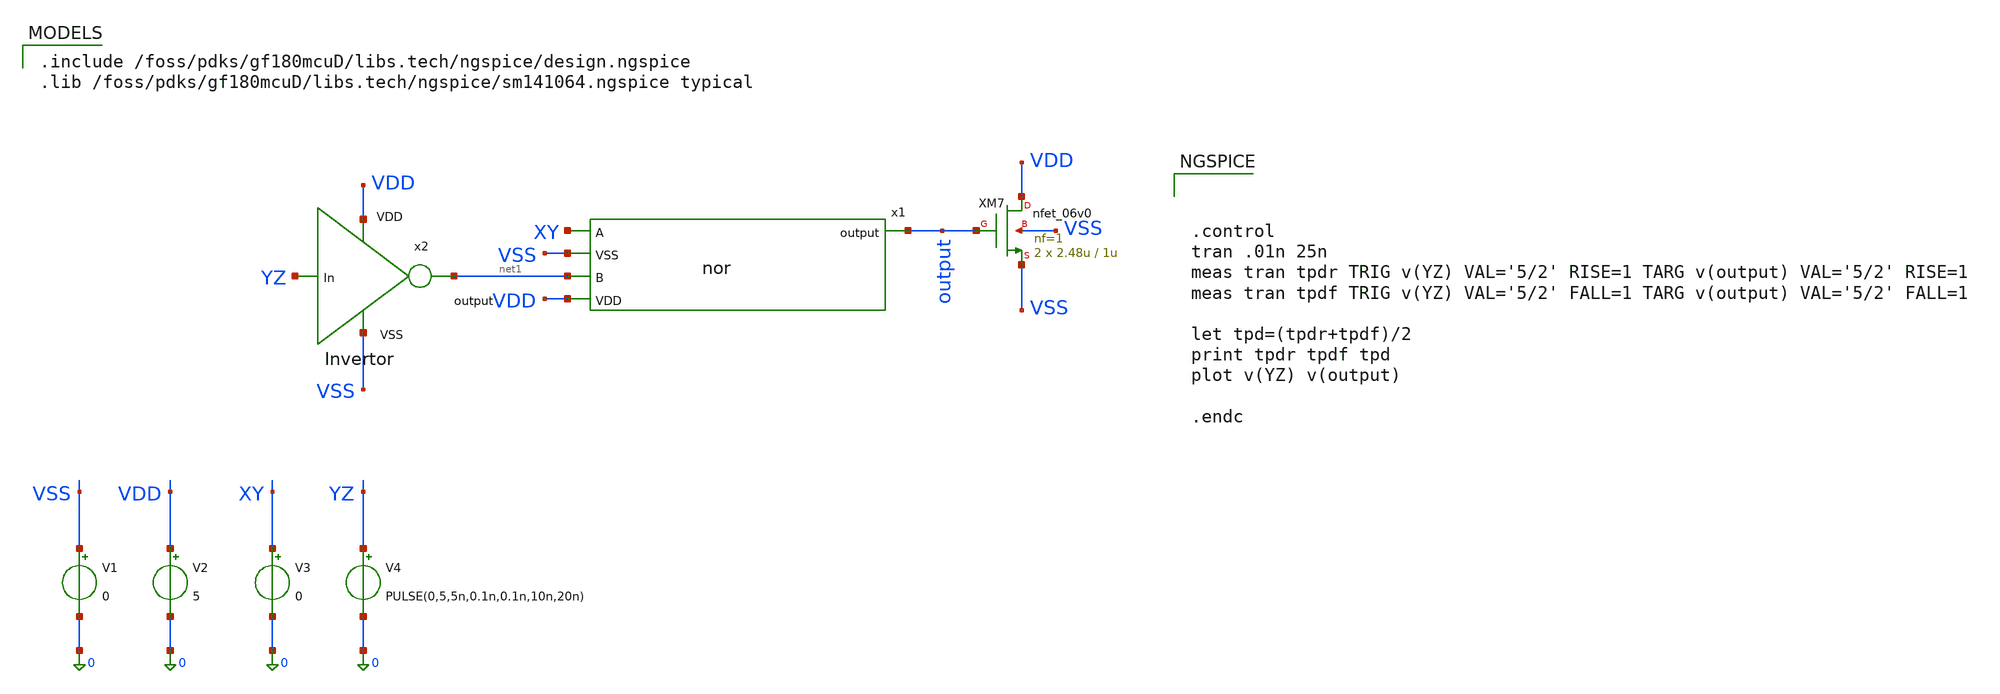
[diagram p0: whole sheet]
** sch_path: activities/opamp3AKAM/yDelayTBV2.sch
**.subckt yDelayTBV2
V1 VSS 0 0
V2 VDD 0 5
V3 XY 0 0
V4 YZ 0 PULSE(0,5,5n,0.1n,0.1n,10n,20n)
x1 XY VSS net1 output VDD nor
x2 VDD net1 YZ VSS invertor
XM7 VDD output VSS VSS nfet_06v0 L=1u W=2.48u nf=1 ad='int((nf+1)/2) * W/nf * 0.18u' as='int((nf+2)/2) * W/nf * 0.18u'
+ pd='2*int((nf+1)/2) * (W/nf + 0.18u)' ps='2*int((nf+2)/2) * (W/nf + 0.18u)' nrd='0.18u / W' nrs='0.18u / W'
+ sa=0 sb=0 sd=0 m=2
**** begin user architecture code

.include /foss/pdks/gf180mcuD/libs.tech/ngspice/design.ngspice
.lib /foss/pdks/gf180mcuD/libs.tech/ngspice/sm141064.ngspice typical




.control
tran .01n 25n
meas tran tpdr TRIG v(YZ) VAL='5/2' RISE=1 TARG v(output) VAL='5/2' RISE=1
meas tran tpdf TRIG v(YZ) VAL='5/2' FALL=1 TARG v(output) VAL='5/2' FALL=1

let tpd=(tpdr+tpdf)/2
print tpdr tpdf tpd
plot v(YZ) v(output)

.endc


**** end user architecture code
**.ends
.end
